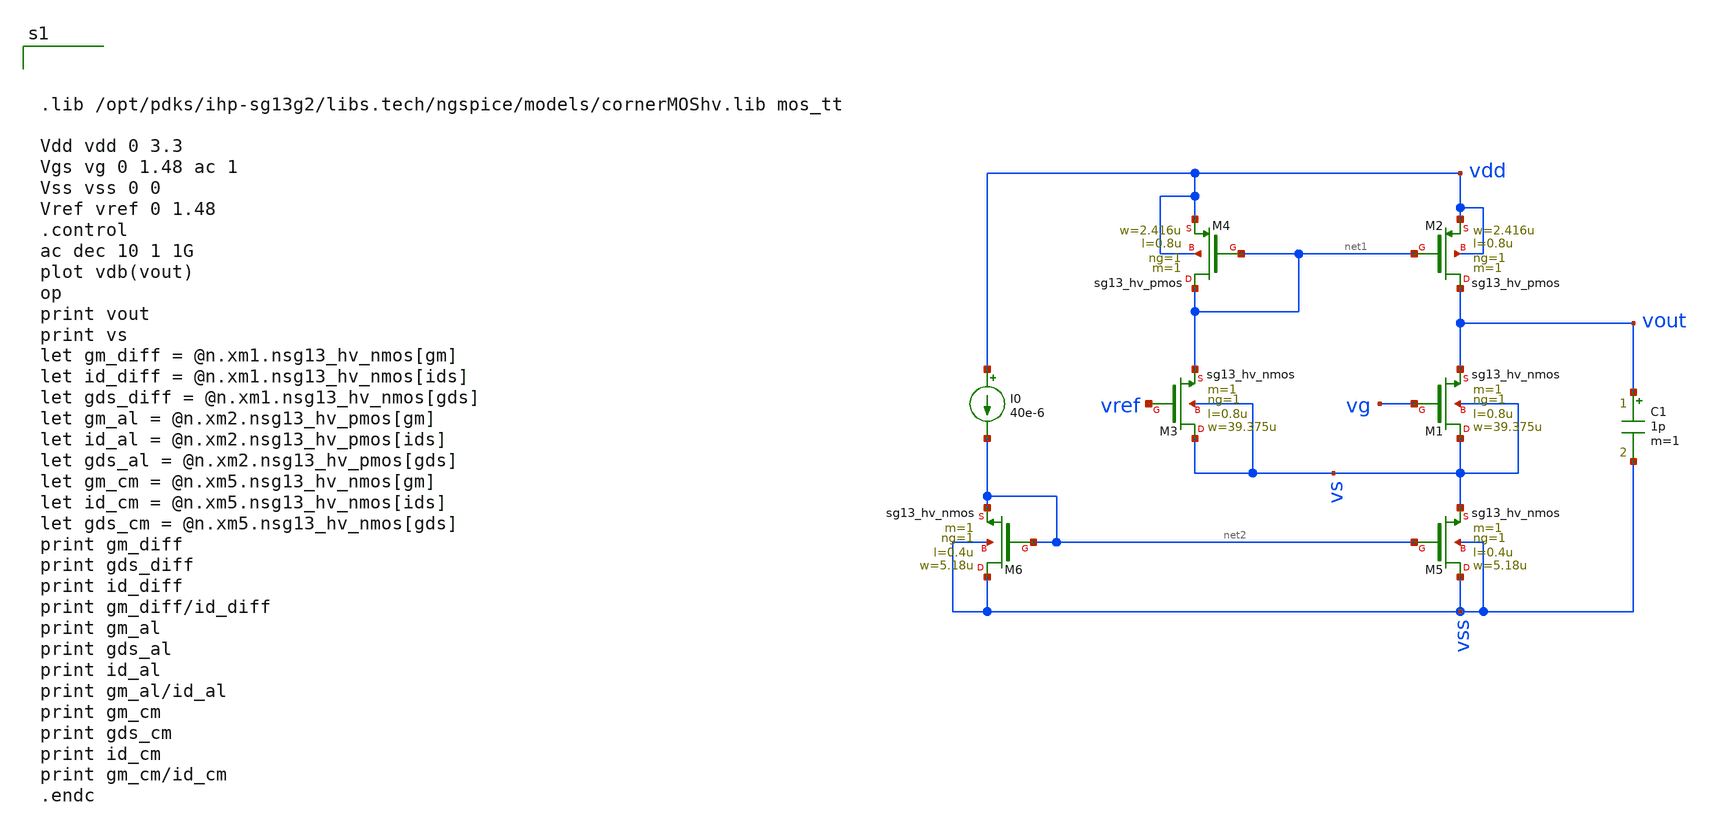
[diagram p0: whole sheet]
** sch_path: test/sstadex/xschem/ihp_test.sch
**.subckt ihp_test
XM1 vs vg vout vs sg13_hv_nmos w=39.375u l=0.8u ng=1 m=1 mm_ok=1
C1 vout vss 1p m=1
XM2 vout net1 vdd vdd sg13_hv_pmos w=2.416u l=0.8u ng=1 m=1 mm_ok=1
XM3 vs vref net1 vs sg13_hv_nmos w=39.375u l=0.8u ng=1 m=1 mm_ok=1
XM4 net1 net1 vdd vdd sg13_hv_pmos w=2.416u l=0.8u ng=1 m=1 mm_ok=1
XM5 vss net2 vs vss sg13_hv_nmos w=5.18u l=0.4u ng=1 m=1 mm_ok=1
XM6 vss net2 net2 vss sg13_hv_nmos w=5.18u l=0.4u ng=1 m=1 mm_ok=1
I0 vdd net2 40e-6
**** begin user architecture code



.lib /opt/pdks/ihp-sg13g2/libs.tech/ngspice/models/cornerMOShv.lib mos_tt

Vdd vdd 0 3.3
Vgs vg 0 1.48 ac 1
Vss vss 0 0
Vref vref 0 1.48
.control
ac dec 10 1 1G
plot vdb(vout)
op
print vout
print vs
let gm_diff = @n.xm1.nsg13_hv_nmos[gm]
let id_diff = @n.xm1.nsg13_hv_nmos[ids]
let gds_diff = @n.xm1.nsg13_hv_nmos[gds]
let gm_al = @n.xm2.nsg13_hv_pmos[gm]
let id_al = @n.xm2.nsg13_hv_pmos[ids]
let gds_al = @n.xm2.nsg13_hv_pmos[gds]
let gm_cm = @n.xm5.nsg13_hv_nmos[gm]
let id_cm = @n.xm5.nsg13_hv_nmos[ids]
let gds_cm = @n.xm5.nsg13_hv_nmos[gds]
print gm_diff
print gds_diff
print id_diff
print gm_diff/id_diff
print gm_al
print gds_al
print id_al
print gm_al/id_al
print gm_cm
print gds_cm
print id_cm
print gm_cm/id_cm
.endc



**** end user architecture code
**.ends
.end
